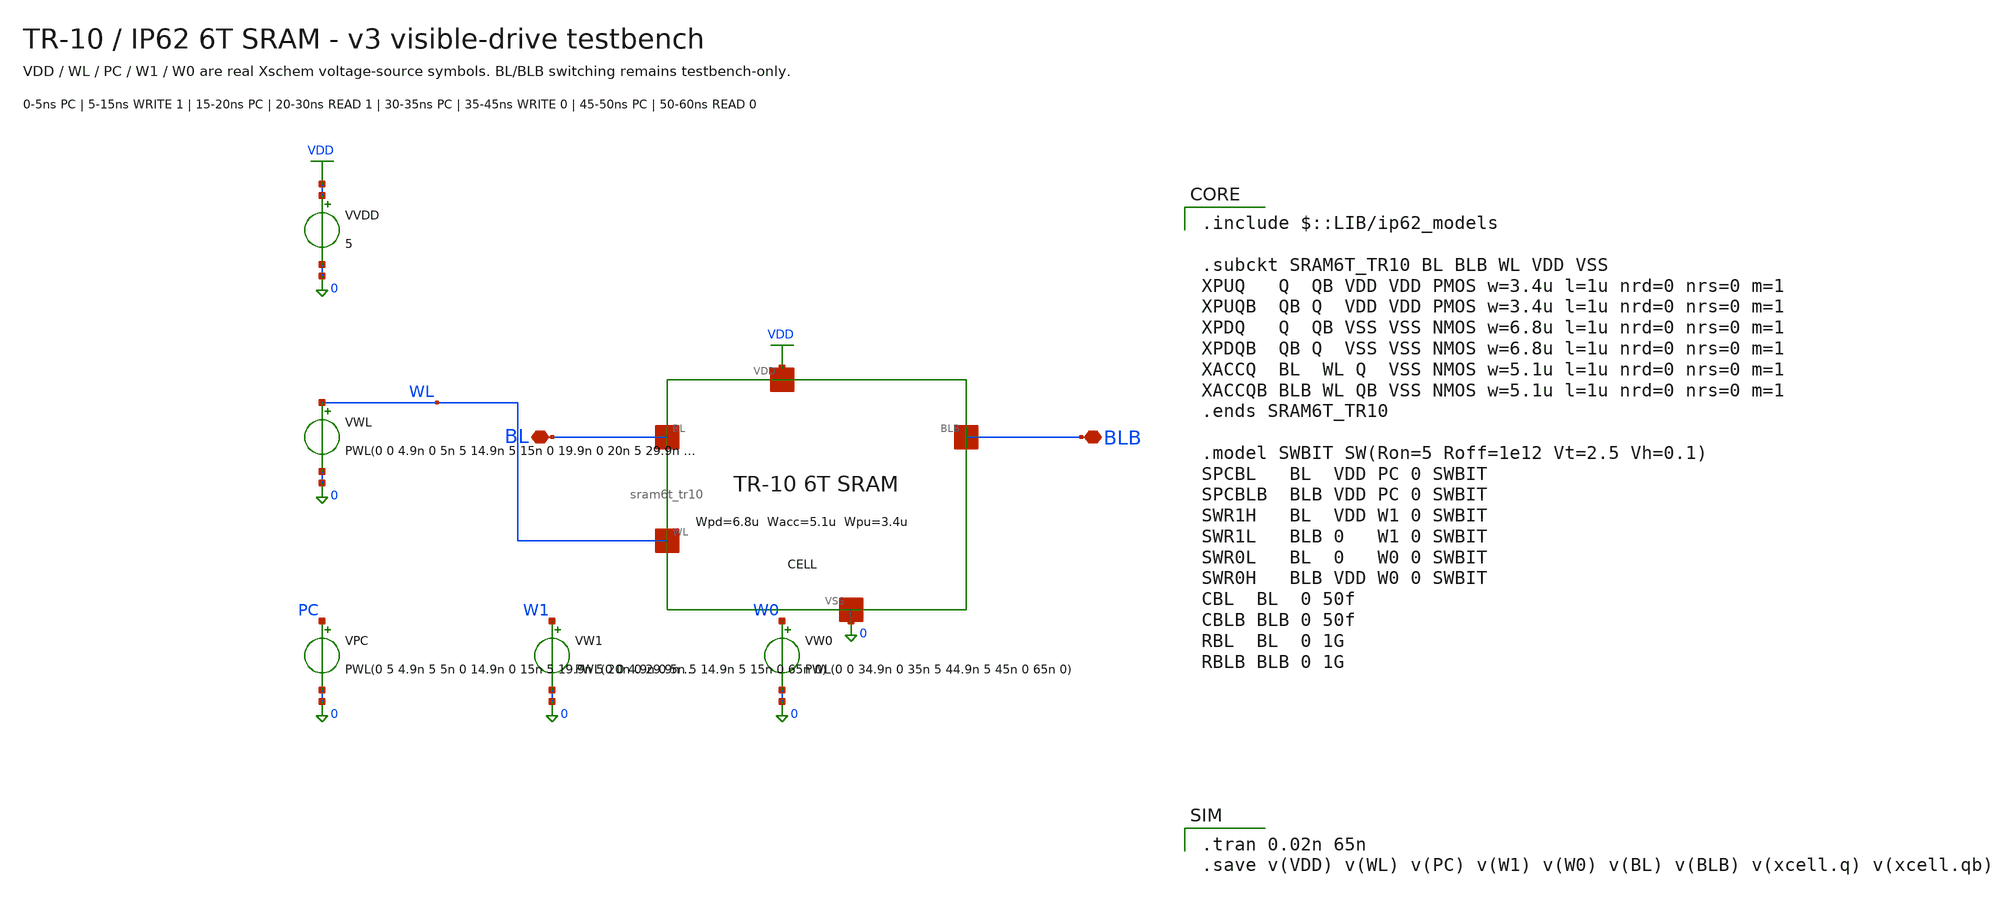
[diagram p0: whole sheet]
** sch_path: generic/tr10_sram6t_v3/tb_sram6t_write_read_v3.sch
**.subckt tb_sram6t_write_read_v3 BL BLB
*.iopin BL
*.iopin BLB
XCELL BL BLB WL net1 0 SRAM6T_TR10
VVDD VDD 0 5
VWL WL 0 PWL(0 0 4.9n 0 5n 5 14.9n 5 15n 0 19.9n 0 20n 5 29.9n 5 30n 0 34.9n 0 35n 5 44.9n 5 45n 0
+ 49.9n 0 50n 5 59.9n 5 60n 0 65n 0)
VPC PC 0 PWL(0 5 4.9n 5 5n 0 14.9n 0 15n 5 19.9n 5 20n 0 29.9n 0 30n 5 34.9n 5 35n 0 44.9n 0 45n 5
+ 49.9n 5 50n 0 59.9n 0 60n 5 65n 5)
VW1 W1 0 PWL(0 0 4.9n 0 5n 5 14.9n 5 15n 0 65n 0)
VW0 W0 0 PWL(0 0 34.9n 0 35n 5 44.9n 5 45n 0 65n 0)
**** begin user architecture code

.include $::LIB/ip62_models

.subckt SRAM6T_TR10 BL BLB WL VDD VSS
XPUQ   Q  QB VDD VDD PMOS w=3.4u l=1u nrd=0 nrs=0 m=1
XPUQB  QB Q  VDD VDD PMOS w=3.4u l=1u nrd=0 nrs=0 m=1
XPDQ   Q  QB VSS VSS NMOS w=6.8u l=1u nrd=0 nrs=0 m=1
XPDQB  QB Q  VSS VSS NMOS w=6.8u l=1u nrd=0 nrs=0 m=1
XACCQ  BL  WL Q  VSS NMOS w=5.1u l=1u nrd=0 nrs=0 m=1
XACCQB BLB WL QB VSS NMOS w=5.1u l=1u nrd=0 nrs=0 m=1
.ends SRAM6T_TR10

.model SWBIT SW(Ron=5 Roff=1e12 Vt=2.5 Vh=0.1)
SPCBL   BL  VDD PC 0 SWBIT
SPCBLB  BLB VDD PC 0 SWBIT
SWR1H   BL  VDD W1 0 SWBIT
SWR1L   BLB 0   W1 0 SWBIT
SWR0L   BL  0   W0 0 SWBIT
SWR0H   BLB VDD W0 0 SWBIT
CBL  BL  0 50f
CBLB BLB 0 50f
RBL  BL  0 1G
RBLB BLB 0 1G


.tran 0.02n 65n
.save v(VDD) v(WL) v(PC) v(W1) v(W0) v(BL) v(BLB) v(xcell.q) v(xcell.qb)

**** end user architecture code
**.ends
.GLOBAL VDD
.end
